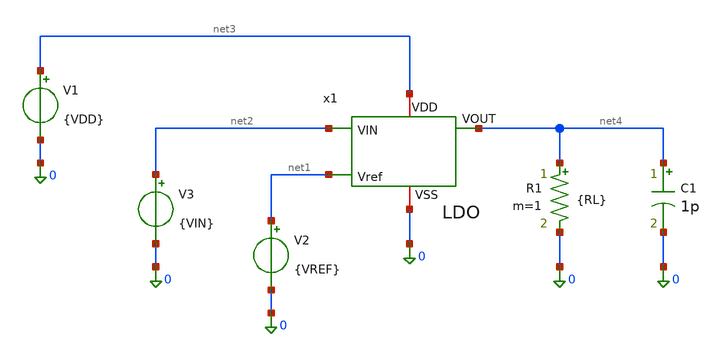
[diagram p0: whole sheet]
** sch_path: xschem/ldo_tb.sch
**.subckt ldo_tb
x1 net2 net4 net3 net1 0 LDO
V1 net3 0 {VDD}
V2 net1 0 {VREF}
V3 net2 0 {VIN}
R1 net4 0 {RL} m=1
C1 net4 0 1p m=1
**.ends

* expanding   symbol:  /foss/designs/LDO-sky130/xschem/LDO.sym # of pins=5
** sym_path: xschem/LDO.sym
** sch_path: xschem/LDO.sch
.subckt LDO VIN VOUT VDD Vref VSS
*.ipin VIN
*.iopin VDD
*.opin VOUT
*.ipin Vref
*.iopin VSS
x1 VDD net2 Vref Vre net1 VSS OTA
I0 VDD net1 10u
XM1 VOUT net2 VIN net3 sky130_fd_pr__pfet_01v8_lvt L=0.35 W=1 nf=1 ad='int((1 + 1)/2) * 1 / 1 * 0.29'
+ as='int((1 + 2)/2) * 1 / 1 * 0.29' pd='2*int((1 + 1)/2) * (1 / 1 + 0.29)' ps='2*int((1 + 2)/2) * (1 / 1 + 0.29)'
+ nrd='0.29 / 1 ' nrs='0.29 / 1 ' sa=0 sb=0 sd=0 mult=1 m=1
XR1 Vre VOUT net4 sky130_fd_pr__res_iso_pw W=2.65 L=2.65 m=1
XR2 VSS Vre net5 sky130_fd_pr__res_iso_pw W=2.65 L=2.65 m=1
.ends


* expanding   symbol:  /foss/designs/LDO-sky130/xschem/OTA.sym # of pins=6
** sym_path: xschem/OTA.sym
** sch_path: xschem/OTA.sch
.subckt OTA VDD VO_ota VIN_ota VIP_ota Iref VSS
*.ipin VIN_ota
*.opin VO_ota
*.iopin Iref
*.iopin VSS
*.iopin VDD
*.ipin VIP_ota
XMr Iref Iref VSS VSS sky130_fd_pr__nfet_01v8 L=0.15 W=1 nf=1 ad='int((1 + 1)/2) * 1 / 1 * 0.29' as='int((1 + 2)/2) * 1 / 1 * 0.29'
+ pd='2*int((1 + 1)/2) * (1 / 1 + 0.29)' ps='2*int((1 + 2)/2) * (1 / 1 + 0.29)' nrd='0.29 / 1 ' nrs='0.29 / 1 '
+ sa=0 sb=0 sd=0 mult=1 m=1
XMo VO_ota VO_ota VDD VDD sky130_fd_pr__pfet_01v8 L=0.15 W=1 nf=1 ad='int((1 + 1)/2) * 1 / 1 * 0.29'
+ as='int((1 + 2)/2) * 1 / 1 * 0.29' pd='2*int((1 + 1)/2) * (1 / 1 + 0.29)' ps='2*int((1 + 2)/2) * (1 / 1 + 0.29)'
+ nrd='0.29 / 1 ' nrs='0.29 / 1 ' sa=0 sb=0 sd=0 mult=1 m=1
XMrc1 Vtail Iref VSS VSS sky130_fd_pr__nfet_01v8 L=0.15 W=1 nf=1 ad='int((1 + 1)/2) * 1 / 1 * 0.29' as='int((1 + 2)/2) * 1 / 1 * 0.29'
+ pd='2*int((1 + 1)/2) * (1 / 1 + 0.29)' ps='2*int((1 + 2)/2) * (1 / 1 + 0.29)' nrd='0.29 / 1 ' nrs='0.29 / 1 '
+ sa=0 sb=0 sd=0 mult=1 m=1
XMc2 VO_ota Iref VSS VSS sky130_fd_pr__nfet_01v8 L=0.15 W=1 nf=1 ad='int((1 + 1)/2) * 1 / 1 * 0.29' as='int((1 + 2)/2) * 1 / 1 * 0.29'
+ pd='2*int((1 + 1)/2) * (1 / 1 + 0.29)' ps='2*int((1 + 2)/2) * (1 / 1 + 0.29)' nrd='0.29 / 1 ' nrs='0.29 / 1 '
+ sa=0 sb=0 sd=0 mult=1 m=1
XMn VGP VIN_ota Vtail VSS sky130_fd_pr__nfet_01v8 L=0.15 W=1 nf=1 ad='int((1 + 1)/2) * 1 / 1 * 0.29'
+ as='int((1 + 2)/2) * 1 / 1 * 0.29' pd='2*int((1 + 1)/2) * (1 / 1 + 0.29)' ps='2*int((1 + 2)/2) * (1 / 1 + 0.29)'
+ nrd='0.29 / 1 ' nrs='0.29 / 1 ' sa=0 sb=0 sd=0 mult=1 m=1
XMp VO_ota VIP_ota Vtail VSS sky130_fd_pr__nfet_01v8 L=0.15 W=1 nf=1 ad='int((1 + 1)/2) * 1 / 1 * 0.29'
+ as='int((1 + 2)/2) * 1 / 1 * 0.29' pd='2*int((1 + 1)/2) * (1 / 1 + 0.29)' ps='2*int((1 + 2)/2) * (1 / 1 + 0.29)'
+ nrd='0.29 / 1 ' nrs='0.29 / 1 ' sa=0 sb=0 sd=0 mult=1 m=1
XMpr VO_ota VGP VDD VDD sky130_fd_pr__pfet_01v8 L=0.15 W=1 nf=1 ad='int((1 + 1)/2) * 1 / 1 * 0.29' as='int((1 + 2)/2) * 1 / 1 * 0.29'
+ pd='2*int((1 + 1)/2) * (1 / 1 + 0.29)' ps='2*int((1 + 2)/2) * (1 / 1 + 0.29)' nrd='0.29 / 1 ' nrs='0.29 / 1 '
+ sa=0 sb=0 sd=0 mult=1 m=1
XMnr VGP VGP VDD VDD sky130_fd_pr__pfet_01v8 L=0.15 W=1 nf=1 ad='int((1 + 1)/2) * 1 / 1 * 0.29' as='int((1 + 2)/2) * 1 / 1 * 0.29'
+ pd='2*int((1 + 1)/2) * (1 / 1 + 0.29)' ps='2*int((1 + 2)/2) * (1 / 1 + 0.29)' nrd='0.29 / 1 ' nrs='0.29 / 1 '
+ sa=0 sb=0 sd=0 mult=1 m=1
.ends

.end
